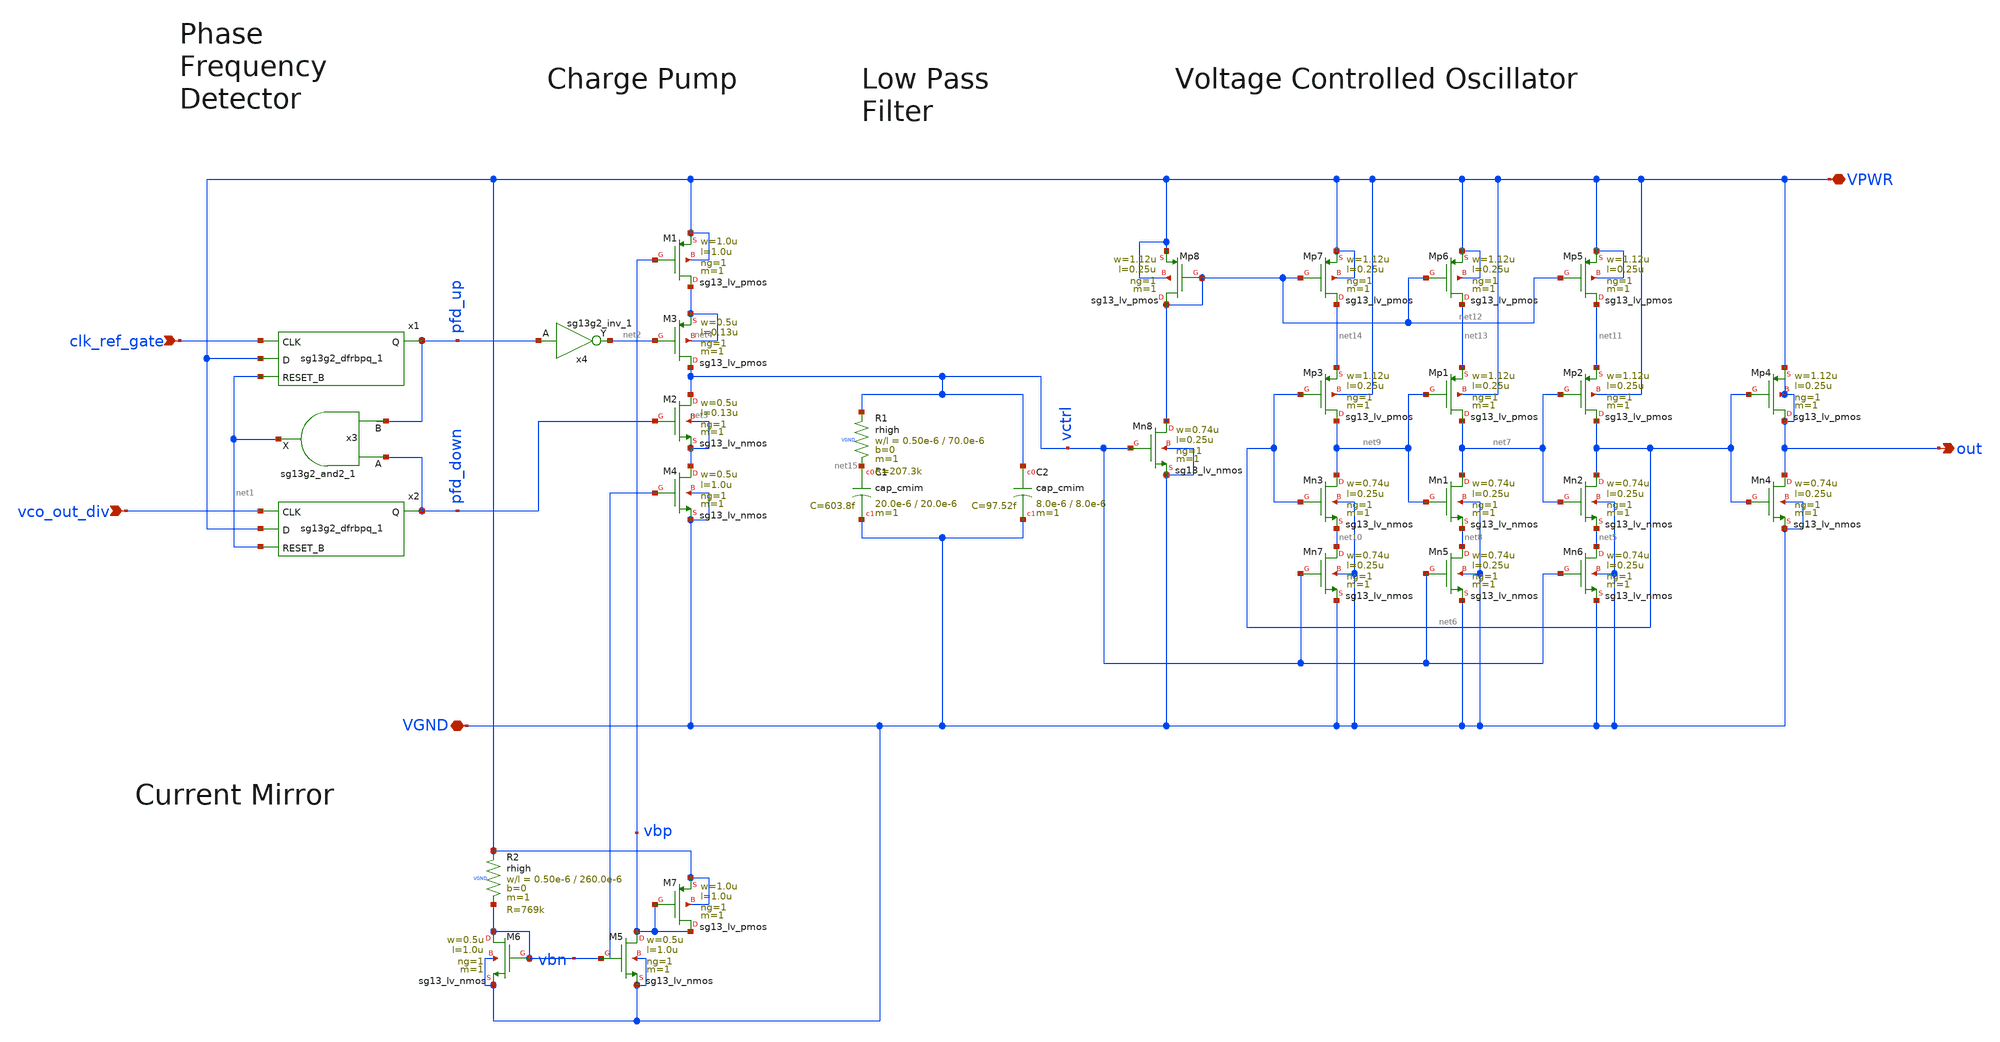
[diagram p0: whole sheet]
** sch_path: analog/pll/schematic/pll_top.sch
**.subckt pll_top clk_ref_gate vco_out_div VGND out VPWR
*.ipin clk_ref_gate
*.ipin vco_out_div
*.iopin VGND
*.opin out
*.iopin VPWR
x1 pfd_up clk_ref_gate VPWR net1 VPWR VGND sg13g2_dfrbpq_1
x2 pfd_down vco_out_div VPWR net1 VPWR VGND sg13g2_dfrbpq_1
x3 net1 pfd_down pfd_up VPWR VGND sg13g2_and2_1
x4 net2 pfd_up VPWR VGND sg13g2_inv_1
XM1 net4 vbp VPWR VPWR sg13_lv_pmos w=1.0u l=1.0u ng=1 m=1 mm_ok=1
XM2 vctrl pfd_down net3 net3 sg13_lv_nmos w=0.5u l=0.13u ng=1 m=1 mm_ok=1
XM3 vctrl net2 net4 net4 sg13_lv_pmos w=0.5u l=0.13u ng=1 m=1 mm_ok=1
XM4 net3 vbn VGND VGND sg13_lv_nmos w=0.5u l=1.0u ng=1 m=1 mm_ok=1
XC1 net15 VGND cap_cmim w=20.0e-6 l=20.0e-6 m=1 mm_ok=1
XR1 vctrl net15 VGND rhigh w=0.50e-6 l=70.0e-6 m=1 b=0 mm_ok=1
XC2 vctrl VGND cap_cmim w=8.0e-6 l=8.0e-6 m=1 mm_ok=1
XMp2 net6 net7 net11 VPWR sg13_lv_pmos w=1.12u l=0.25u ng=1 m=1 mm_ok=1
XMn2 net6 net7 net5 VGND sg13_lv_nmos w=0.74u l=0.25u ng=1 m=1 mm_ok=1
XMp1 net7 net9 net13 VPWR sg13_lv_pmos w=1.12u l=0.25u ng=1 m=1 mm_ok=1
XMn1 net7 net9 net8 VGND sg13_lv_nmos w=0.74u l=0.25u ng=1 m=1 mm_ok=1
XMp3 net9 net6 net14 VPWR sg13_lv_pmos w=1.12u l=0.25u ng=1 m=1 mm_ok=1
XMn3 net9 net6 net10 VGND sg13_lv_nmos w=0.74u l=0.25u ng=1 m=1 mm_ok=1
XMp4 out net6 VPWR out sg13_lv_pmos w=1.12u l=0.25u ng=1 m=1 mm_ok=1
XMn4 out net6 VGND VGND sg13_lv_nmos w=0.74u l=0.25u ng=1 m=1 mm_ok=1
XMp5 net11 net12 VPWR VPWR sg13_lv_pmos w=1.12u l=0.25u ng=1 m=1 mm_ok=1
XMp6 net13 net12 VPWR VPWR sg13_lv_pmos w=1.12u l=0.25u ng=1 m=1 mm_ok=1
XMp7 net14 net12 VPWR VPWR sg13_lv_pmos w=1.12u l=0.25u ng=1 m=1 mm_ok=1
XMn5 net8 vctrl VGND VGND sg13_lv_nmos w=0.74u l=0.25u ng=1 m=1 mm_ok=1
XMn6 net5 vctrl VGND VGND sg13_lv_nmos w=0.74u l=0.25u ng=1 m=1 mm_ok=1
XMn7 net10 vctrl VGND VGND sg13_lv_nmos w=0.74u l=0.25u ng=1 m=1 mm_ok=1
XMp8 net12 net12 VPWR VPWR sg13_lv_pmos w=1.12u l=0.25u ng=1 m=1 mm_ok=1
XMn8 net12 vctrl VGND VGND sg13_lv_nmos w=0.74u l=0.25u ng=1 m=1 mm_ok=1
XM5 vbp vbn VGND VGND sg13_lv_nmos w=0.5u l=1.0u ng=1 m=1 mm_ok=1
XM6 vbn vbn VGND VGND sg13_lv_nmos w=0.5u l=1.0u ng=1 m=1 mm_ok=1
XM7 vbp vbp VPWR VPWR sg13_lv_pmos w=1.0u l=1.0u ng=1 m=1 mm_ok=1
XR2 VPWR vbn VGND rhigh w=0.50e-6 l=260.0e-6 m=1 b=0 mm_ok=1
**.ends

* expanding   symbol:  sg13g2_dfrbpq_1.sym # of pins=4
** sym_path: sg13g2_dfrbpq_1.sym
** sch_path: sg13g2_dfrbpq_1.sch
.subckt sg13g2_dfrbpq_1 Q CLK D RESET_B VDD VSS
*.opin Q
*.ipin CLK
*.ipin D
*.ipin RESET_B
*.iopin VDD
*.iopin VSS
XM1 Db D net10 VSS sg13_lv_nmos w=420.00n l=130.00n ng=1 m=1 mm_ok=1
XM2 net10 RESET_B VSS VSS sg13_lv_nmos w=420.00n l=130.00n ng=1 m=1 mm_ok=1
XM3 net1 clkneg net9 VSS sg13_lv_nmos w=420.00n l=130.00n ng=1 m=1 mm_ok=1
XM4 net9 net1 VSS VSS sg13_lv_nmos w=420.00n l=130.00n ng=1 m=1 mm_ok=1
XM5 net1 net1 net5 VSS sg13_lv_nmos w=420.00n l=130.00n ng=1 m=1 mm_ok=1
XM6 net5 RESET_B VSS VSS sg13_lv_nmos w=420.00n l=130.00n ng=1 m=1 mm_ok=1
XM7 net2 net1 VSS VSS sg13_lv_nmos w=740.00n l=130.00n ng=1 m=1 mm_ok=1
XM8 Q net2 VSS VSS sg13_lv_nmos w=740.00n l=130.00n ng=1 m=1 mm_ok=1
XM9 clkneg CLK VSS VSS sg13_lv_nmos w=740.00n l=130.00n ng=1 m=1 mm_ok=1
XM10 clkpos clkneg VSS VSS sg13_lv_nmos w=740.00n l=130.00n ng=1 m=1 mm_ok=1
XM11 Db clkneg net3 VSS sg13_lv_nmos w=420.00n l=130.00n ng=1 m=1 mm_ok=1
XM12 net3 clkpos net8 VSS sg13_lv_nmos w=420.00n l=130.00n ng=1 m=1 mm_ok=1
XM13 net8 net3 net4 VSS sg13_lv_nmos w=420.00n l=130.00n ng=1 m=1 mm_ok=1
XM14 net4 RESET_B VSS VSS sg13_lv_nmos w=420.00n l=130.00n ng=1 m=1 mm_ok=1
XM15 net3 net3 VSS VSS sg13_lv_nmos w=740.00n l=130.00n ng=1 m=1 mm_ok=1
XM16 net3 clkpos net1 VSS sg13_lv_nmos w=740.00n l=130.00n ng=1 m=1 mm_ok=1
XM17 Db RESET_B VDD VDD sg13_lv_pmos w=420.00n l=130.00n ng=1 m=1 mm_ok=1
XM18 Db D VDD VDD sg13_lv_pmos w=420.00n l=130.00n ng=1 m=1 mm_ok=1
XM19 net7 net1 VDD VDD sg13_lv_pmos w=420.00n l=130.00n ng=1 m=1 mm_ok=1
XM20 net1 clkpos net7 VDD sg13_lv_pmos w=420.00n l=130.00n ng=1 m=1 mm_ok=1
XM21 net1 net1 VDD VDD sg13_lv_pmos w=420.00n l=130.00n ng=1 m=1 mm_ok=1
XM22 net1 RESET_B VDD VDD sg13_lv_pmos w=420.00n l=130.00n ng=1 m=1 mm_ok=1
XM23 net2 net1 VDD VDD sg13_lv_pmos w=1.12u l=130.00n ng=1 m=1 mm_ok=1
XM24 Q net2 VDD VDD sg13_lv_pmos w=1.12u l=130.00n ng=1 m=1 mm_ok=1
XM25 clkneg CLK VDD VDD sg13_lv_pmos w=1.12u l=130.00n ng=1 m=1 mm_ok=1
XM26 clkpos clkneg VDD VDD sg13_lv_pmos w=1.12u l=130.00n ng=1 m=1 mm_ok=1
XM27 Db clkpos net3 VDD sg13_lv_pmos w=420.00n l=130.00n ng=1 m=1 mm_ok=1
XM28 net6 net3 VDD VDD sg13_lv_pmos w=420.00n l=130.00n ng=1 m=1 mm_ok=1
XM29 net3 clkneg net6 VDD sg13_lv_pmos w=420.00n l=130.00n ng=1 m=1 mm_ok=1
XM30 net3 RESET_B VDD VDD sg13_lv_pmos w=420.00n l=130.00n ng=1 m=1 mm_ok=1
XM31 net3 net3 VDD VDD sg13_lv_pmos w=1.000u l=130.00n ng=1 m=1 mm_ok=1
XM32 net3 clkneg net1 VDD sg13_lv_pmos w=1.000u l=130.00n ng=1 m=1 mm_ok=1
.ends


* expanding   symbol:  sg13g2_and2_1.sym # of pins=3
** sym_path: sg13g2_and2_1.sym
** sch_path: sg13g2_and2_1.sch
.subckt sg13g2_and2_1 X A B VDD VSS
*.ipin A
*.ipin B
*.opin X
*.iopin VDD
*.iopin VSS
XM1 net1 A net2 VSS sg13_lv_nmos w=640.00n l=130.00n ng=1 m=1 mm_ok=1
XM2 net2 B VSS VSS sg13_lv_nmos w=640.00n l=130.00n ng=1 m=1 mm_ok=1
XM3 X net1 VSS VSS sg13_lv_nmos w=740.00n l=130.00n ng=1 m=1 mm_ok=1
XM4 net1 B VDD VDD sg13_lv_pmos w=840.00n l=130.00n ng=1 m=1 mm_ok=1
XM5 net1 A VDD VDD sg13_lv_pmos w=840.00n l=130.00n ng=1 m=1 mm_ok=1
XM6 X net1 VDD VDD sg13_lv_pmos w=1.12u l=130.00n ng=1 m=1 mm_ok=1
.ends


* expanding   symbol:  sg13g2_inv_1.sym # of pins=2
** sym_path: sg13g2_inv_1.sym
** sch_path: sg13g2_inv_1.sch
.subckt sg13g2_inv_1 Y A VDD VSS
*.opin Y
*.ipin A
*.iopin VDD
*.iopin VSS
XM1 Y A VSS VSS sg13_lv_nmos w=740.00n l=130.00n ng=1 m=1 mm_ok=1
XM2 Y A VDD VDD sg13_lv_pmos w=1.12u l=130.00n ng=1 m=1 mm_ok=1
.ends

.end
